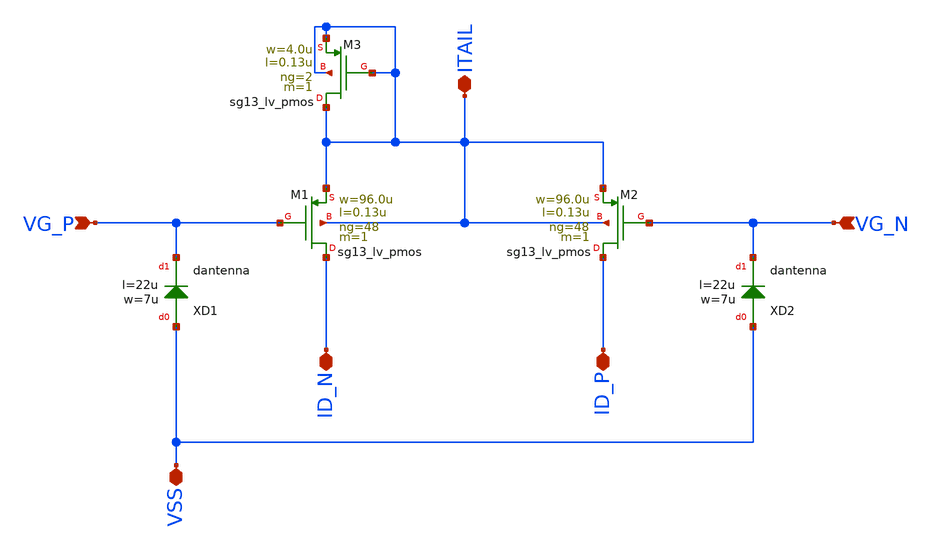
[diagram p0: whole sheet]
** sch_path: JKU_TC1/design_data/sfl-test-cells/xschem/diffpairs/dp_p_100u_130n.sch
**.subckt dp_p_100u_130n VG_P VG_N ITAIL ID_N ID_P VSS
*.ipin VG_P
*.ipin VG_N
*.iopin ITAIL
*.iopin ID_N
*.iopin ID_P
*.iopin VSS
XM1 ID_N VG_P ITAIL ITAIL sg13_lv_pmos w=96.0u l=0.13u ng=48 m=1 mm_ok=1
XM2 ID_P VG_N ITAIL ITAIL sg13_lv_pmos w=96.0u l=0.13u ng=48 m=1 mm_ok=1
XM3 ITAIL ITAIL ITAIL ITAIL sg13_lv_pmos w=4.0u l=0.13u ng=2 m=1 mm_ok=1
XXD1 VSS VG_P dantenna l=22u w=7u
XXD2 VSS VG_N dantenna l=22u w=7u
**.ends
.end
